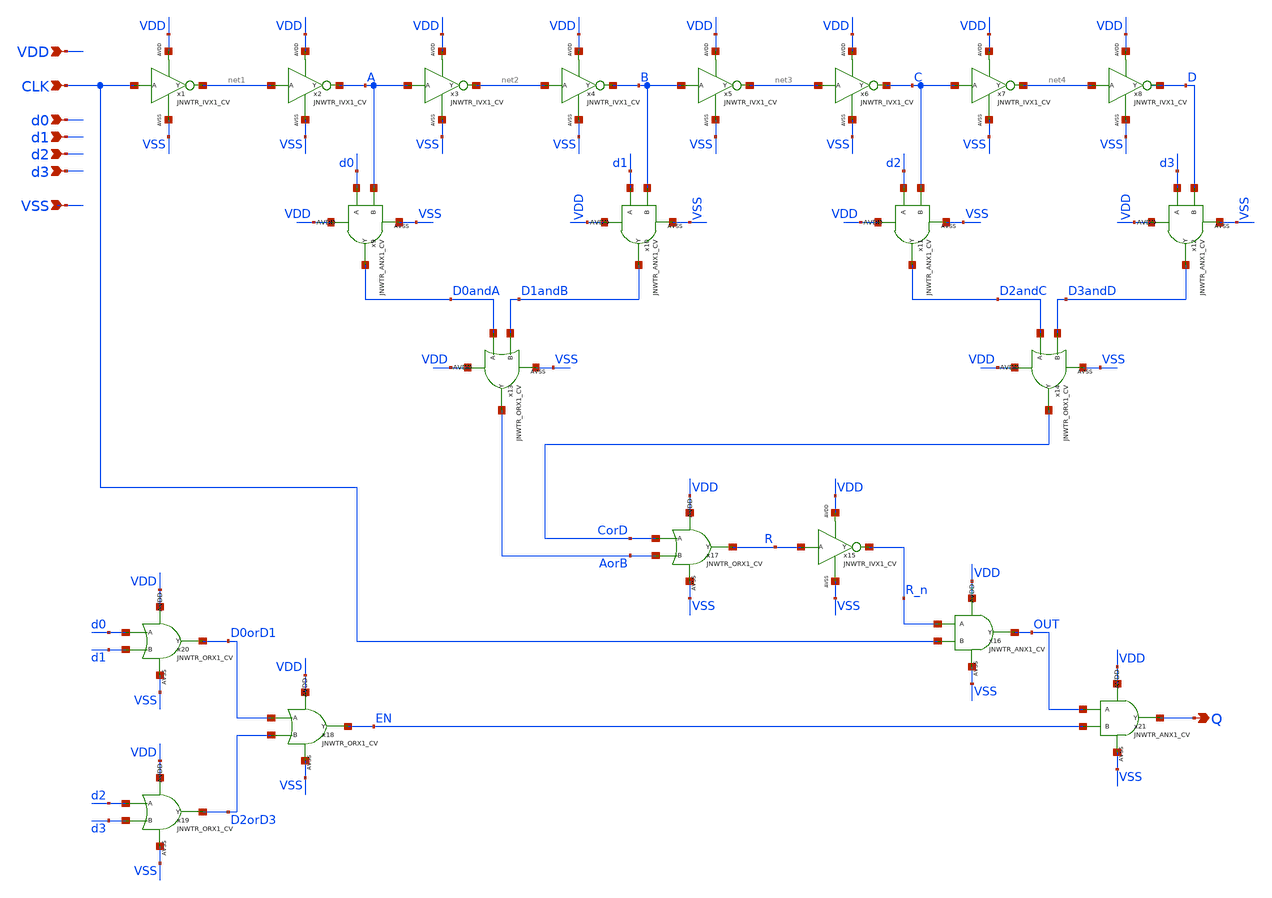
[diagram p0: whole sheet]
** sch_path: design/LELO_TORD_SKY130A/dig-to-time.sch
**.subckt dig-to-time CLK VDD VSS d0 d2 d1 d3 Q
*.ipin CLK
*.ipin VDD
*.ipin VSS
*.ipin d0
*.ipin d2
*.ipin d1
*.ipin d3
*.opin Q
x1 CLK net1 VDD VSS JNWTR_IVX1_CV
x2 net1 A VDD VSS JNWTR_IVX1_CV
x3 A net2 VDD VSS JNWTR_IVX1_CV
x4 net2 B VDD VSS JNWTR_IVX1_CV
x5 B net3 VDD VSS JNWTR_IVX1_CV
x6 net3 C VDD VSS JNWTR_IVX1_CV
x7 C net4 VDD VSS JNWTR_IVX1_CV
x8 net4 D VDD VSS JNWTR_IVX1_CV
x11 d2 C D2andC VDD VSS JNWTR_ANX1_CV xoffset=0 yoffset=0 angle=0 M=1
x9 d0 A D0andA VDD VSS JNWTR_ANX1_CV xoffset=0 yoffset=0 angle=0 M=1
x17 CorD AorB R VDD VSS JNWTR_ORX1_CV xoffset=0 yoffset=0 angle=0 M=1
x14 D2andC D3andD CorD VDD VSS JNWTR_ORX1_CV xoffset=0 yoffset=0 angle=0 M=1
x10 d1 B D1andB VDD VSS JNWTR_ANX1_CV xoffset=0 yoffset=0 angle=0 M=1
x12 d3 D D3andD VDD VSS JNWTR_ANX1_CV xoffset=0 yoffset=0 angle=0 M=1
x13 D0andA D1andB AorB VDD VSS JNWTR_ORX1_CV xoffset=0 yoffset=0 angle=0 M=1
x15 R R_n VDD VSS JNWTR_IVX1_CV
x16 R_n CLK OUT VDD VSS JNWTR_ANX1_CV xoffset=0 yoffset=0 angle=0 M=1
x18 D0orD1 D2orD3 EN VDD VSS JNWTR_ORX1_CV xoffset=0 yoffset=0 angle=0 M=1
x19 d2 d3 D2orD3 VDD VSS JNWTR_ORX1_CV xoffset=0 yoffset=0 angle=0 M=1
x20 d0 d1 D0orD1 VDD VSS JNWTR_ORX1_CV xoffset=0 yoffset=0 angle=0 M=1
x21 OUT EN Q VDD VSS JNWTR_ANX1_CV xoffset=0 yoffset=0 angle=0 M=1
**.ends
.end
